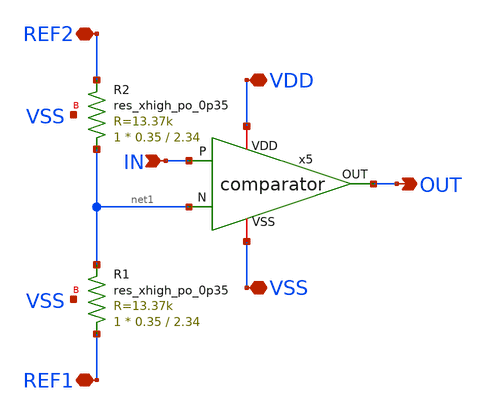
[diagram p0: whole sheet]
** sch_path: xschem/ladder_rung.sch
**.subckt ladder_rung OUT VDD VSS IN REF1 REF2
*.opin OUT
*.iopin VDD
*.iopin VSS
*.ipin IN
*.iopin REF1
*.iopin REF2
XR1 REF1 net1 VSS sky130_fd_pr__res_xhigh_po_0p35 L=2.34 mult=1 m=1
x5 VDD OUT IN net1 VSS comparator
XR2 net1 REF2 VSS sky130_fd_pr__res_xhigh_po_0p35 L=2.34 mult=1 m=1
**.ends

* expanding   symbol:  comparator.sym # of pins=5
** sym_path: xschem/comparator.sym
** sch_path: xschem/comparator.sch
.subckt comparator VDD OUT P N VSS
*.iopin VDD
*.iopin VSS
*.ipin P
*.ipin N
*.opin OUT
x1 VDD net1 P N VSS opamp
x2 VDD OUT net1 VSS buffer
.ends


* expanding   symbol:  opamp.sym # of pins=5
** sym_path: xschem/opamp.sym
** sch_path: xschem/opamp.sch
.subckt opamp VDD OUT P N VSS
*.iopin VDD
*.iopin VSS
*.ipin P
*.ipin N
*.opin OUT
XR1 net2 VDD VSS sky130_fd_pr__res_xhigh_po_0p35 L=24.36 mult=1 m=1
XM1 net2 net2 VSS VSS sky130_fd_pr__nfet_g5v0d10v5 L=1 W=2 nf=1 ad='int((nf+1)/2) * W/nf * 0.29' as='int((nf+2)/2) * W/nf * 0.29'
+ pd='2*int((nf+1)/2) * (W/nf + 0.29)' ps='2*int((nf+2)/2) * (W/nf + 0.29)' nrd='0.29 / W' nrs='0.29 / W'
+ sa=0 sb=0 sd=0 mult=2 m=2
XM7 net1 net1 VDD VDD sky130_fd_pr__pfet_g5v0d10v5 L=1 W=4 nf=1 ad='int((nf+1)/2) * W/nf * 0.29' as='int((nf+2)/2) * W/nf * 0.29'
+ pd='2*int((nf+1)/2) * (W/nf + 0.29)' ps='2*int((nf+2)/2) * (W/nf + 0.29)' nrd='0.29 / W' nrs='0.29 / W'
+ sa=0 sb=0 sd=0 mult=2 m=2
XM8 OUT net1 VDD VDD sky130_fd_pr__pfet_g5v0d10v5 L=1 W=4 nf=1 ad='int((nf+1)/2) * W/nf * 0.29' as='int((nf+2)/2) * W/nf * 0.29'
+ pd='2*int((nf+1)/2) * (W/nf + 0.29)' ps='2*int((nf+2)/2) * (W/nf + 0.29)' nrd='0.29 / W' nrs='0.29 / W'
+ sa=0 sb=0 sd=0 mult=2 m=2
XM4 net6 net2 VSS VSS sky130_fd_pr__nfet_g5v0d10v5 L=1 W=2 nf=1 ad='int((nf+1)/2) * W/nf * 0.29' as='int((nf+2)/2) * W/nf * 0.29'
+ pd='2*int((nf+1)/2) * (W/nf + 0.29)' ps='2*int((nf+2)/2) * (W/nf + 0.29)' nrd='0.29 / W' nrs='0.29 / W'
+ sa=0 sb=0 sd=0 mult=2 m=2
XM5 net1 P net6 VSS sky130_fd_pr__nfet_g5v0d10v5 L=1 W=2 nf=1 ad='int((nf+1)/2) * W/nf * 0.29' as='int((nf+2)/2) * W/nf * 0.29'
+ pd='2*int((nf+1)/2) * (W/nf + 0.29)' ps='2*int((nf+2)/2) * (W/nf + 0.29)' nrd='0.29 / W' nrs='0.29 / W'
+ sa=0 sb=0 sd=0 mult=2 m=2
XM6 OUT N net6 VSS sky130_fd_pr__nfet_g5v0d10v5 L=1 W=2 nf=1 ad='int((nf+1)/2) * W/nf * 0.29' as='int((nf+2)/2) * W/nf * 0.29'
+ pd='2*int((nf+1)/2) * (W/nf + 0.29)' ps='2*int((nf+2)/2) * (W/nf + 0.29)' nrd='0.29 / W' nrs='0.29 / W'
+ sa=0 sb=0 sd=0 mult=2 m=2
XM2 net5 net2 VSS VSS sky130_fd_pr__nfet_g5v0d10v5 L=1 W=2 nf=1 ad='int((nf+1)/2) * W/nf * 0.29' as='int((nf+2)/2) * W/nf * 0.29'
+ pd='2*int((nf+1)/2) * (W/nf + 0.29)' ps='2*int((nf+2)/2) * (W/nf + 0.29)' nrd='0.29 / W' nrs='0.29 / W'
+ sa=0 sb=0 sd=0 mult=2 m=2
XM9 net4 net5 VDD VDD sky130_fd_pr__pfet_g5v0d10v5 L=1 W=4 nf=1 ad='int((nf+1)/2) * W/nf * 0.29' as='int((nf+2)/2) * W/nf * 0.29'
+ pd='2*int((nf+1)/2) * (W/nf + 0.29)' ps='2*int((nf+2)/2) * (W/nf + 0.29)' nrd='0.29 / W' nrs='0.29 / W'
+ sa=0 sb=0 sd=0 mult=2 m=2
XM3 VDD net5 net5 VDD sky130_fd_pr__pfet_g5v0d10v5 L=1 W=4 nf=1 ad='int((nf+1)/2) * W/nf * 0.29' as='int((nf+2)/2) * W/nf * 0.29'
+ pd='2*int((nf+1)/2) * (W/nf + 0.29)' ps='2*int((nf+2)/2) * (W/nf + 0.29)' nrd='0.29 / W' nrs='0.29 / W'
+ sa=0 sb=0 sd=0 mult=2 m=2
XM10 net3 P net4 VDD sky130_fd_pr__pfet_g5v0d10v5 L=1 W=4 nf=1 ad='int((nf+1)/2) * W/nf * 0.29' as='int((nf+2)/2) * W/nf * 0.29'
+ pd='2*int((nf+1)/2) * (W/nf + 0.29)' ps='2*int((nf+2)/2) * (W/nf + 0.29)' nrd='0.29 / W' nrs='0.29 / W'
+ sa=0 sb=0 sd=0 mult=2 m=2
XM11 OUT N net4 VDD sky130_fd_pr__pfet_g5v0d10v5 L=1 W=4 nf=1 ad='int((nf+1)/2) * W/nf * 0.29' as='int((nf+2)/2) * W/nf * 0.29'
+ pd='2*int((nf+1)/2) * (W/nf + 0.29)' ps='2*int((nf+2)/2) * (W/nf + 0.29)' nrd='0.29 / W' nrs='0.29 / W'
+ sa=0 sb=0 sd=0 mult=2 m=2
XM12 net3 net3 VSS VSS sky130_fd_pr__nfet_g5v0d10v5 L=1 W=2 nf=1 ad='int((nf+1)/2) * W/nf * 0.29' as='int((nf+2)/2) * W/nf * 0.29'
+ pd='2*int((nf+1)/2) * (W/nf + 0.29)' ps='2*int((nf+2)/2) * (W/nf + 0.29)' nrd='0.29 / W' nrs='0.29 / W'
+ sa=0 sb=0 sd=0 mult=2 m=2
XM13 OUT net3 VSS VSS sky130_fd_pr__nfet_g5v0d10v5 L=1 W=2 nf=1 ad='int((nf+1)/2) * W/nf * 0.29' as='int((nf+2)/2) * W/nf * 0.29'
+ pd='2*int((nf+1)/2) * (W/nf + 0.29)' ps='2*int((nf+2)/2) * (W/nf + 0.29)' nrd='0.29 / W' nrs='0.29 / W'
+ sa=0 sb=0 sd=0 mult=2 m=2
.ends


* expanding   symbol:  buffer.sym # of pins=4
** sym_path: xschem/buffer.sym
** sch_path: xschem/buffer.sch
.subckt buffer VDD OUT IN VSS
*.iopin VDD
*.iopin VSS
*.ipin IN
*.opin OUT
XM1 net1 IN VSS VSS sky130_fd_pr__nfet_g5v0d10v5 L=0.5 W=0.5 nf=1 ad='int((nf+1)/2) * W/nf * 0.29' as='int((nf+2)/2) * W/nf * 0.29'
+ pd='2*int((nf+1)/2) * (W/nf + 0.29)' ps='2*int((nf+2)/2) * (W/nf + 0.29)' nrd='0.29 / W' nrs='0.29 / W'
+ sa=0 sb=0 sd=0 mult=1 m=1
XM2 net1 IN VDD VDD sky130_fd_pr__pfet_g5v0d10v5 L=0.5 W=1 nf=1 ad='int((nf+1)/2) * W/nf * 0.29' as='int((nf+2)/2) * W/nf * 0.29'
+ pd='2*int((nf+1)/2) * (W/nf + 0.29)' ps='2*int((nf+2)/2) * (W/nf + 0.29)' nrd='0.29 / W' nrs='0.29 / W'
+ sa=0 sb=0 sd=0 mult=1 m=1
XM3 OUT net1 VSS VSS sky130_fd_pr__nfet_g5v0d10v5 L=0.5 W=0.5 nf=1 ad='int((nf+1)/2) * W/nf * 0.29' as='int((nf+2)/2) * W/nf * 0.29'
+ pd='2*int((nf+1)/2) * (W/nf + 0.29)' ps='2*int((nf+2)/2) * (W/nf + 0.29)' nrd='0.29 / W' nrs='0.29 / W'
+ sa=0 sb=0 sd=0 mult=1 m=1
XM4 OUT net1 VDD VDD sky130_fd_pr__pfet_g5v0d10v5 L=0.5 W=1 nf=1 ad='int((nf+1)/2) * W/nf * 0.29' as='int((nf+2)/2) * W/nf * 0.29'
+ pd='2*int((nf+1)/2) * (W/nf + 0.29)' ps='2*int((nf+2)/2) * (W/nf + 0.29)' nrd='0.29 / W' nrs='0.29 / W'
+ sa=0 sb=0 sd=0 mult=1 m=1
.ends

.end
